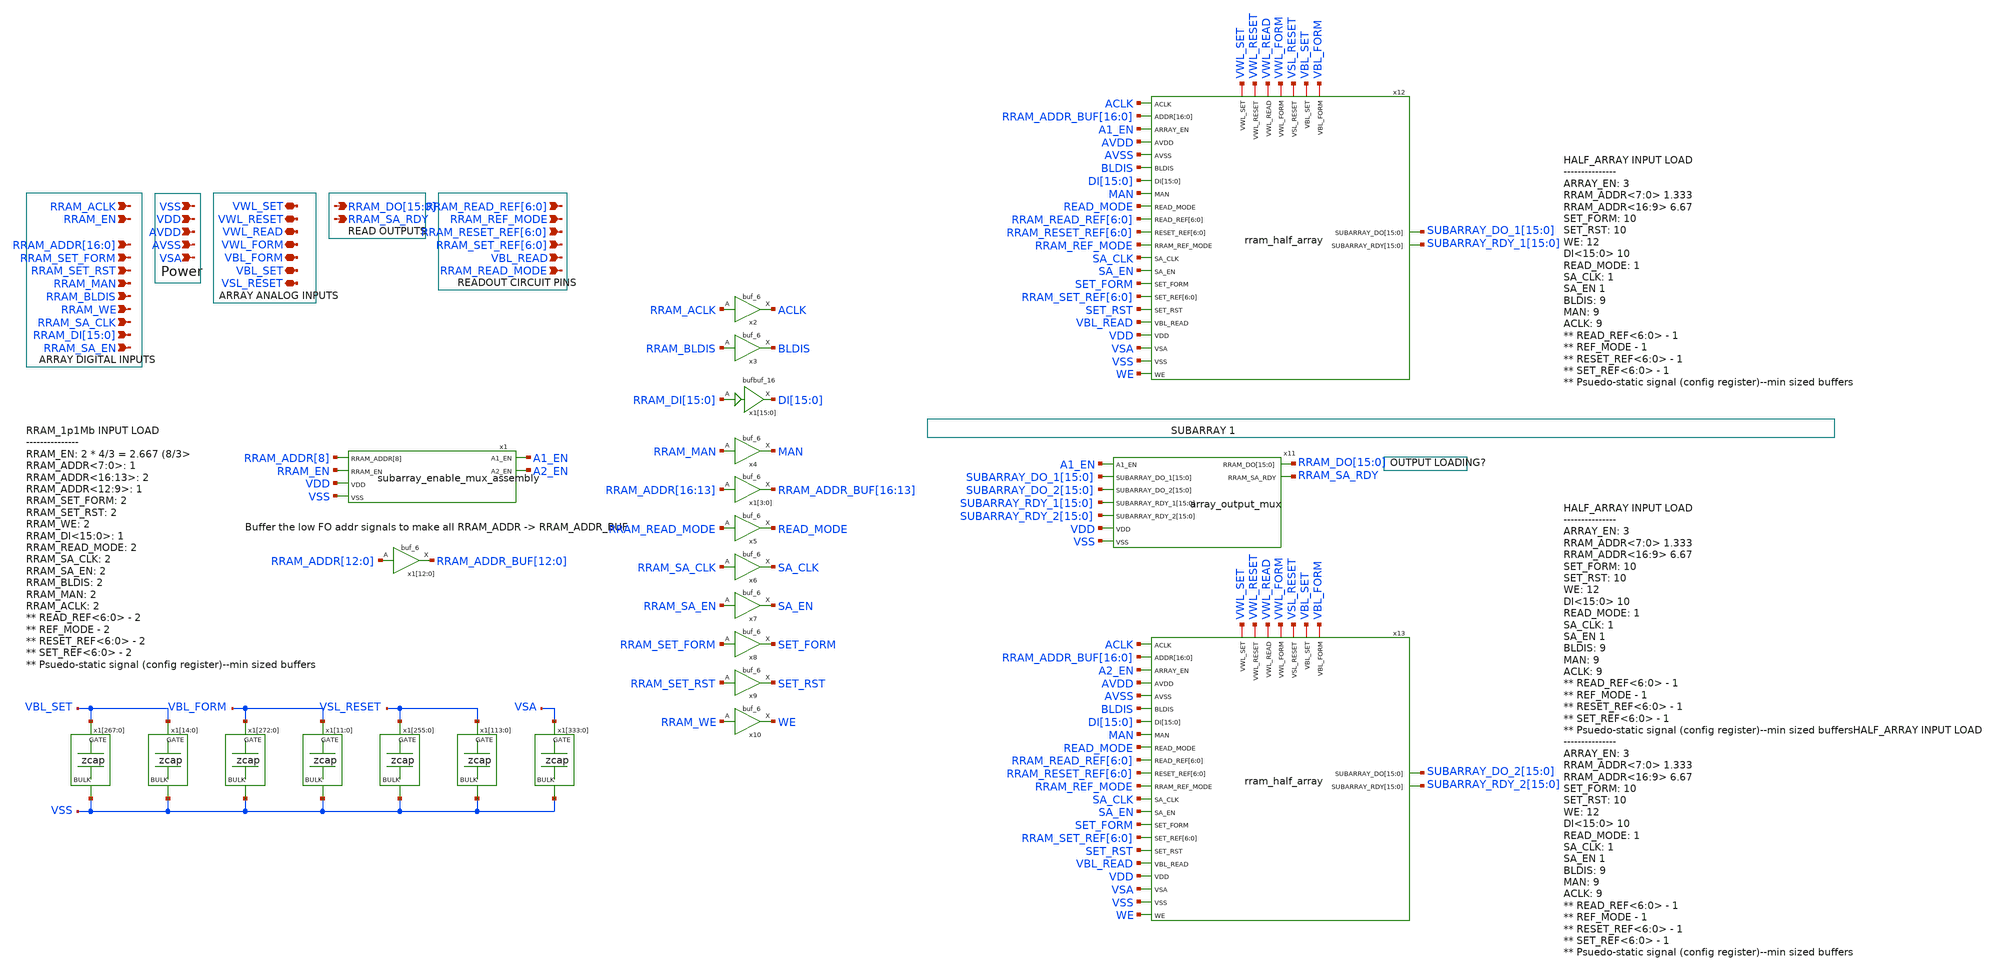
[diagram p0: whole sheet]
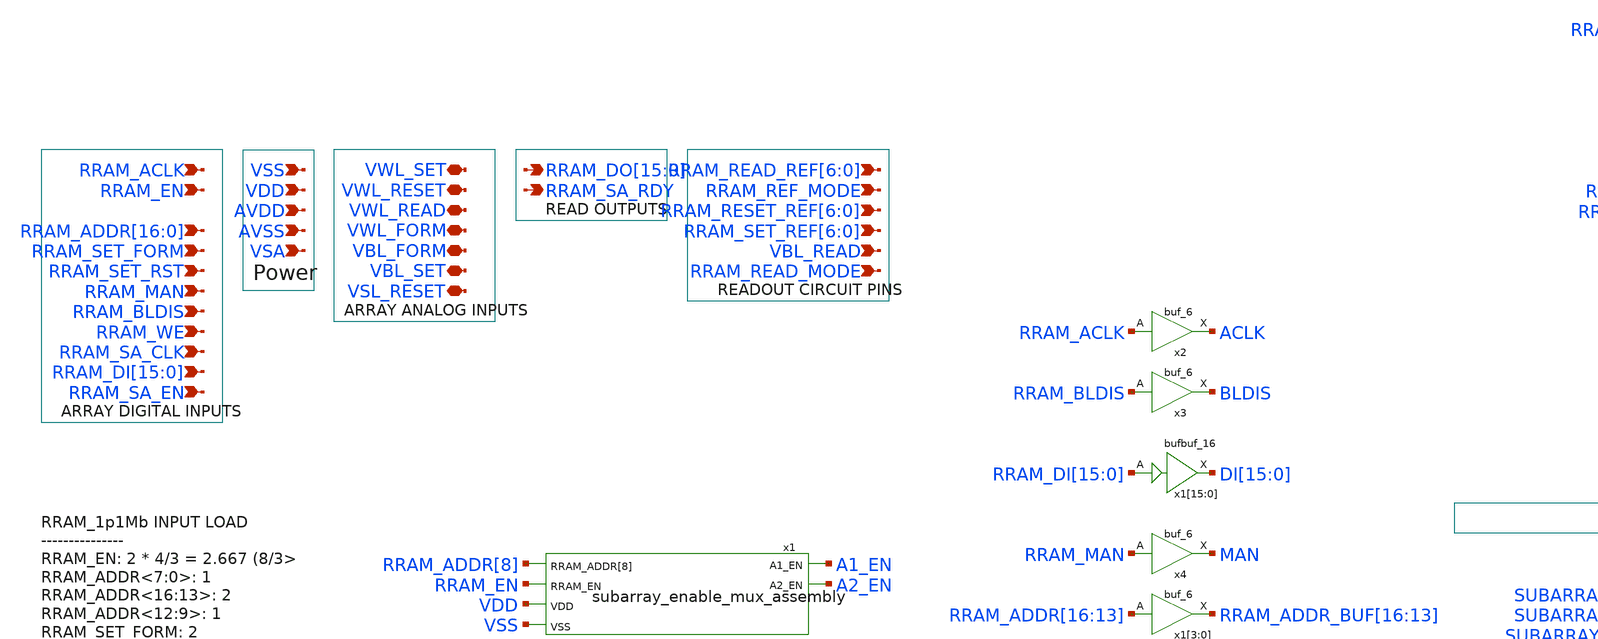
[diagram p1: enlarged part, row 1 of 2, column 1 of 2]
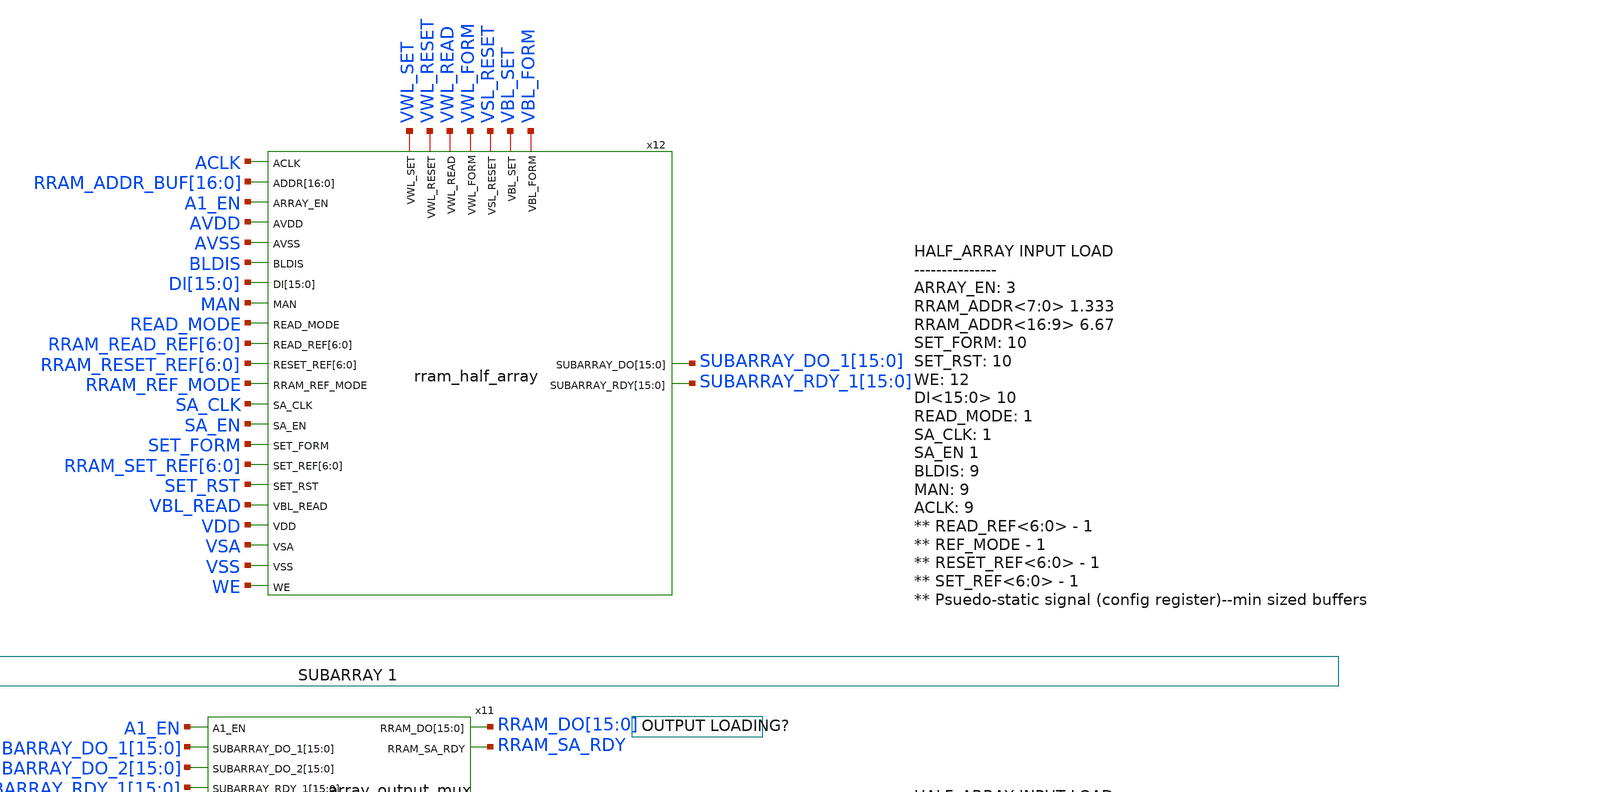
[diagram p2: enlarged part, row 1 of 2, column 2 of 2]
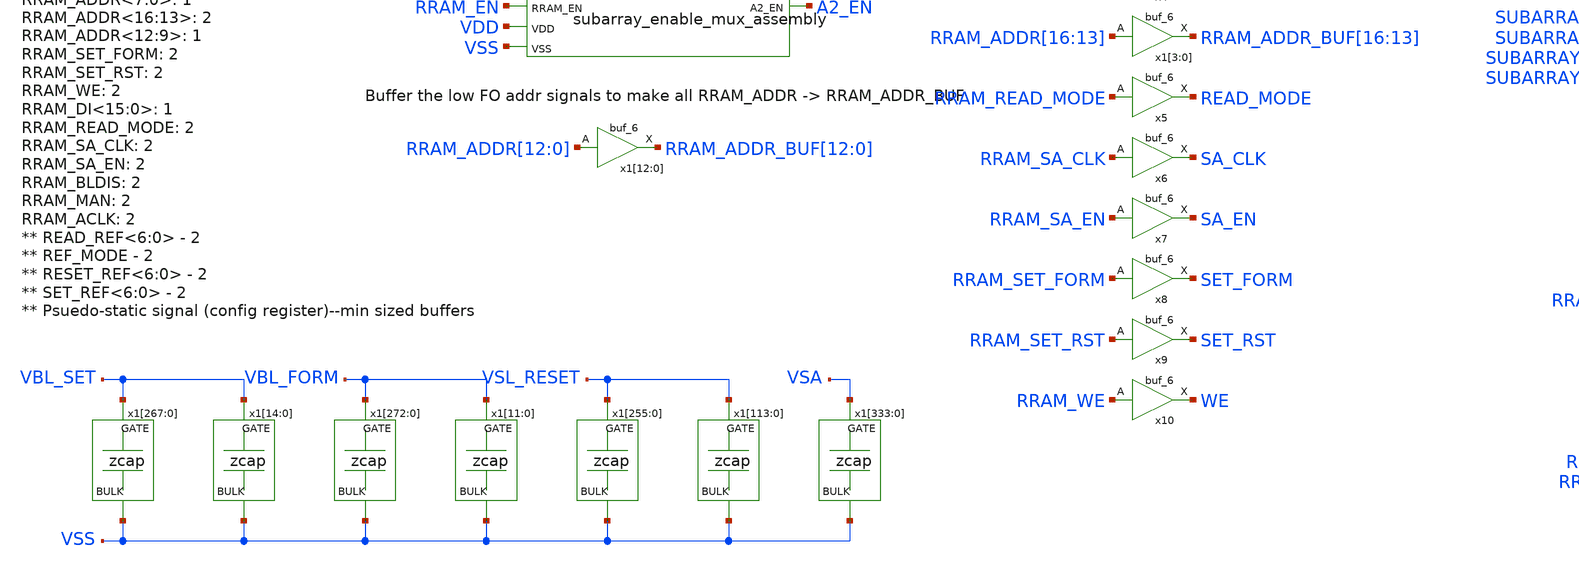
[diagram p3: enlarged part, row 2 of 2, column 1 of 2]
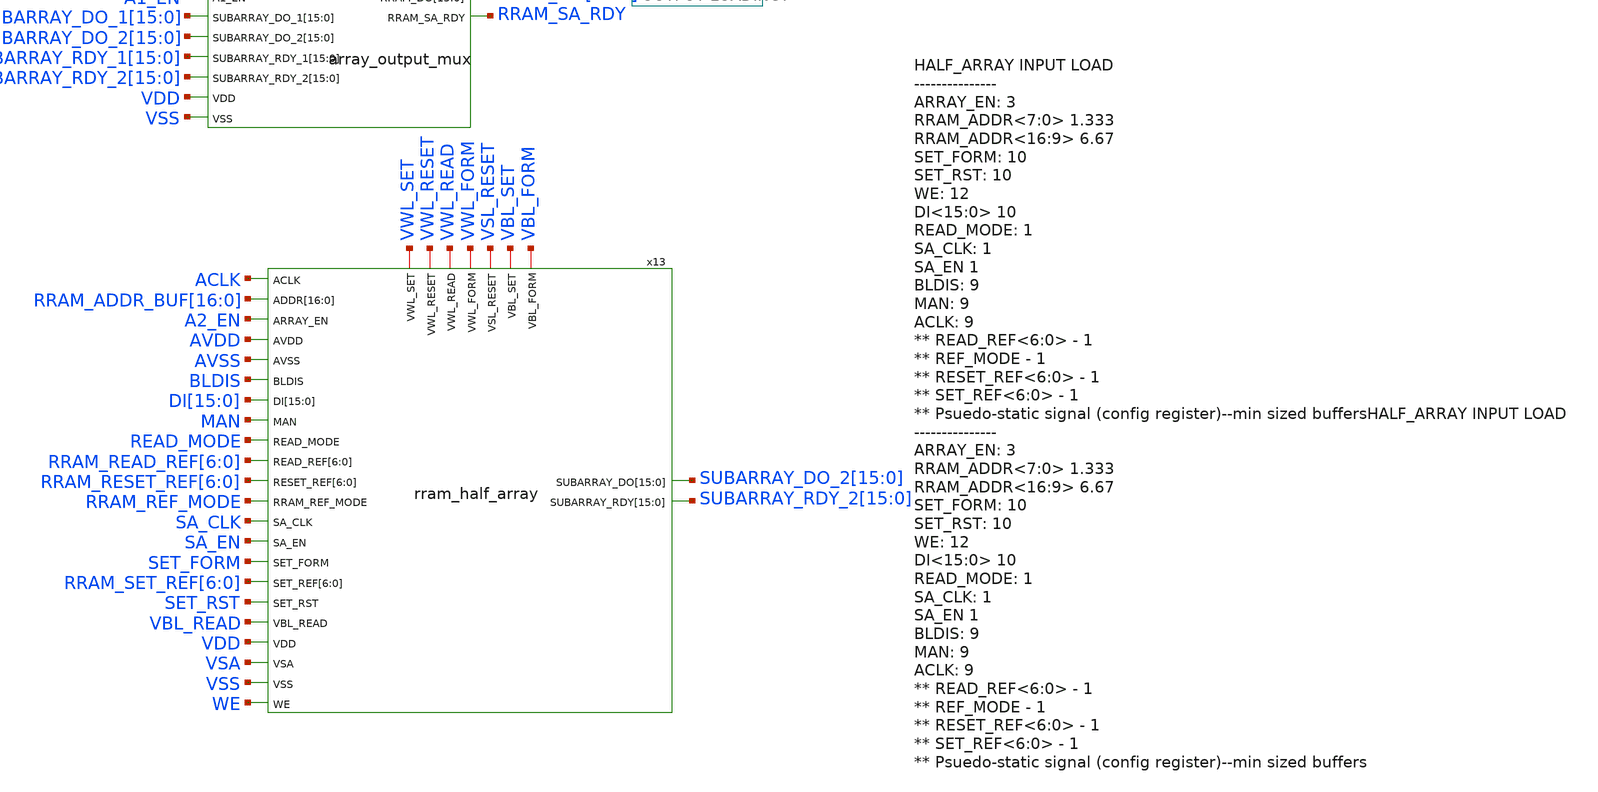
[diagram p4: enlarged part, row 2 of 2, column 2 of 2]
** sch_path: Top_Level_Array/rram_1pMb.sch
**.subckt rram_1pMb RRAM_ACLK RRAM_EN
*+ RRAM_ADDR[16],RRAM_ADDR[15],RRAM_ADDR[14],RRAM_ADDR[13],RRAM_ADDR[12],RRAM_ADDR[11],RRAM_ADDR[10],RRAM_ADDR[9],RRAM_ADDR[8],RRAM_ADDR[7],RRAM_ADDR[6],RRAM_ADDR[5],RRAM_ADDR[4],RRAM_ADDR[3],RRAM_ADDR[2],RRAM_ADDR[1],RRAM_ADDR[0] RRAM_SET_FORM RRAM_SET_RST RRAM_MAN RRAM_BLDIS RRAM_WE RRAM_SA_CLK
*+ RRAM_DI[15],RRAM_DI[14],RRAM_DI[13],RRAM_DI[12],RRAM_DI[11],RRAM_DI[10],RRAM_DI[9],RRAM_DI[8],RRAM_DI[7],RRAM_DI[6],RRAM_DI[5],RRAM_DI[4],RRAM_DI[3],RRAM_DI[2],RRAM_DI[1],RRAM_DI[0] RRAM_SA_EN VSS VDD AVDD AVSS VSA VWL_SET VWL_RESET VWL_READ VWL_FORM VBL_FORM VBL_SET VSL_RESET
*+ RRAM_DO[15],RRAM_DO[14],RRAM_DO[13],RRAM_DO[12],RRAM_DO[11],RRAM_DO[10],RRAM_DO[9],RRAM_DO[8],RRAM_DO[7],RRAM_DO[6],RRAM_DO[5],RRAM_DO[4],RRAM_DO[3],RRAM_DO[2],RRAM_DO[1],RRAM_DO[0] RRAM_SA_RDY
*+ RRAM_READ_REF[6],RRAM_READ_REF[5],RRAM_READ_REF[4],RRAM_READ_REF[3],RRAM_READ_REF[2],RRAM_READ_REF[1],RRAM_READ_REF[0] RRAM_REF_MODE
*+ RRAM_RESET_REF[6],RRAM_RESET_REF[5],RRAM_RESET_REF[4],RRAM_RESET_REF[3],RRAM_RESET_REF[2],RRAM_RESET_REF[1],RRAM_RESET_REF[0]
*+ RRAM_SET_REF[6],RRAM_SET_REF[5],RRAM_SET_REF[4],RRAM_SET_REF[3],RRAM_SET_REF[2],RRAM_SET_REF[1],RRAM_SET_REF[0] VBL_READ RRAM_READ_MODE
*.ipin RRAM_ACLK
*.ipin RRAM_EN
*.ipin
*+ RRAM_ADDR[16],RRAM_ADDR[15],RRAM_ADDR[14],RRAM_ADDR[13],RRAM_ADDR[12],RRAM_ADDR[11],RRAM_ADDR[10],RRAM_ADDR[9],RRAM_ADDR[8],RRAM_ADDR[7],RRAM_ADDR[6],RRAM_ADDR[5],RRAM_ADDR[4],RRAM_ADDR[3],RRAM_ADDR[2],RRAM_ADDR[1],RRAM_ADDR[0]
*.ipin RRAM_SET_FORM
*.ipin RRAM_SET_RST
*.ipin RRAM_MAN
*.ipin RRAM_BLDIS
*.ipin RRAM_WE
*.ipin RRAM_SA_CLK
*.ipin
*+ RRAM_DI[15],RRAM_DI[14],RRAM_DI[13],RRAM_DI[12],RRAM_DI[11],RRAM_DI[10],RRAM_DI[9],RRAM_DI[8],RRAM_DI[7],RRAM_DI[6],RRAM_DI[5],RRAM_DI[4],RRAM_DI[3],RRAM_DI[2],RRAM_DI[1],RRAM_DI[0]
*.ipin RRAM_SA_EN
*.ipin VSS
*.ipin VDD
*.ipin AVDD
*.ipin AVSS
*.ipin VSA
*.iopin VWL_SET
*.iopin VWL_RESET
*.iopin VWL_READ
*.iopin VWL_FORM
*.iopin VBL_FORM
*.iopin VBL_SET
*.iopin VSL_RESET
*.opin
*+ RRAM_DO[15],RRAM_DO[14],RRAM_DO[13],RRAM_DO[12],RRAM_DO[11],RRAM_DO[10],RRAM_DO[9],RRAM_DO[8],RRAM_DO[7],RRAM_DO[6],RRAM_DO[5],RRAM_DO[4],RRAM_DO[3],RRAM_DO[2],RRAM_DO[1],RRAM_DO[0]
*.opin RRAM_SA_RDY
*.ipin
*+ RRAM_READ_REF[6],RRAM_READ_REF[5],RRAM_READ_REF[4],RRAM_READ_REF[3],RRAM_READ_REF[2],RRAM_READ_REF[1],RRAM_READ_REF[0]
*.ipin RRAM_REF_MODE
*.ipin
*+ RRAM_RESET_REF[6],RRAM_RESET_REF[5],RRAM_RESET_REF[4],RRAM_RESET_REF[3],RRAM_RESET_REF[2],RRAM_RESET_REF[1],RRAM_RESET_REF[0]
*.ipin
*+ RRAM_SET_REF[6],RRAM_SET_REF[5],RRAM_SET_REF[4],RRAM_SET_REF[3],RRAM_SET_REF[2],RRAM_SET_REF[1],RRAM_SET_REF[0]
*.ipin VBL_READ
*.ipin RRAM_READ_MODE
x1[12] RRAM_ADDR[12] VSS VSS VDD VDD RRAM_ADDR_BUF[12] sky130_fd_sc_hd__buf_6
x1[11] RRAM_ADDR[11] VSS VSS VDD VDD RRAM_ADDR_BUF[11] sky130_fd_sc_hd__buf_6
x1[10] RRAM_ADDR[10] VSS VSS VDD VDD RRAM_ADDR_BUF[10] sky130_fd_sc_hd__buf_6
x1[9] RRAM_ADDR[9] VSS VSS VDD VDD RRAM_ADDR_BUF[9] sky130_fd_sc_hd__buf_6
x1[8] RRAM_ADDR[8] VSS VSS VDD VDD RRAM_ADDR_BUF[8] sky130_fd_sc_hd__buf_6
x1[7] RRAM_ADDR[7] VSS VSS VDD VDD RRAM_ADDR_BUF[7] sky130_fd_sc_hd__buf_6
x1[6] RRAM_ADDR[6] VSS VSS VDD VDD RRAM_ADDR_BUF[6] sky130_fd_sc_hd__buf_6
x1[5] RRAM_ADDR[5] VSS VSS VDD VDD RRAM_ADDR_BUF[5] sky130_fd_sc_hd__buf_6
x1[4] RRAM_ADDR[4] VSS VSS VDD VDD RRAM_ADDR_BUF[4] sky130_fd_sc_hd__buf_6
x1[3] RRAM_ADDR[3] VSS VSS VDD VDD RRAM_ADDR_BUF[3] sky130_fd_sc_hd__buf_6
x1[2] RRAM_ADDR[2] VSS VSS VDD VDD RRAM_ADDR_BUF[2] sky130_fd_sc_hd__buf_6
x1[1] RRAM_ADDR[1] VSS VSS VDD VDD RRAM_ADDR_BUF[1] sky130_fd_sc_hd__buf_6
x1[0] RRAM_ADDR[0] VSS VSS VDD VDD RRAM_ADDR_BUF[0] sky130_fd_sc_hd__buf_6
x1 VSS VDD A1_EN RRAM_EN RRAM_ADDR[8] A2_EN subarray_enable_mux_assembly
x1[15] RRAM_DI[15] VSS VSS VDD VDD DI[15] sky130_fd_sc_hd__bufbuf_16
x1[14] RRAM_DI[14] VSS VSS VDD VDD DI[14] sky130_fd_sc_hd__bufbuf_16
x1[13] RRAM_DI[13] VSS VSS VDD VDD DI[13] sky130_fd_sc_hd__bufbuf_16
x1[12] RRAM_DI[12] VSS VSS VDD VDD DI[12] sky130_fd_sc_hd__bufbuf_16
x1[11] RRAM_DI[11] VSS VSS VDD VDD DI[11] sky130_fd_sc_hd__bufbuf_16
x1[10] RRAM_DI[10] VSS VSS VDD VDD DI[10] sky130_fd_sc_hd__bufbuf_16
x1[9] RRAM_DI[9] VSS VSS VDD VDD DI[9] sky130_fd_sc_hd__bufbuf_16
x1[8] RRAM_DI[8] VSS VSS VDD VDD DI[8] sky130_fd_sc_hd__bufbuf_16
x1[7] RRAM_DI[7] VSS VSS VDD VDD DI[7] sky130_fd_sc_hd__bufbuf_16
x1[6] RRAM_DI[6] VSS VSS VDD VDD DI[6] sky130_fd_sc_hd__bufbuf_16
x1[5] RRAM_DI[5] VSS VSS VDD VDD DI[5] sky130_fd_sc_hd__bufbuf_16
x1[4] RRAM_DI[4] VSS VSS VDD VDD DI[4] sky130_fd_sc_hd__bufbuf_16
x1[3] RRAM_DI[3] VSS VSS VDD VDD DI[3] sky130_fd_sc_hd__bufbuf_16
x1[2] RRAM_DI[2] VSS VSS VDD VDD DI[2] sky130_fd_sc_hd__bufbuf_16
x1[1] RRAM_DI[1] VSS VSS VDD VDD DI[1] sky130_fd_sc_hd__bufbuf_16
x1[0] RRAM_DI[0] VSS VSS VDD VDD DI[0] sky130_fd_sc_hd__bufbuf_16
x2 RRAM_ACLK VSS VSS VDD VDD ACLK sky130_fd_sc_hd__buf_6
x3 RRAM_BLDIS VSS VSS VDD VDD BLDIS sky130_fd_sc_hd__buf_6
x4 RRAM_MAN VSS VSS VDD VDD MAN sky130_fd_sc_hd__buf_6
x1[3] RRAM_ADDR[16] VSS VSS VDD VDD RRAM_ADDR_BUF[16] sky130_fd_sc_hd__buf_6
x1[2] RRAM_ADDR[15] VSS VSS VDD VDD RRAM_ADDR_BUF[15] sky130_fd_sc_hd__buf_6
x1[1] RRAM_ADDR[14] VSS VSS VDD VDD RRAM_ADDR_BUF[14] sky130_fd_sc_hd__buf_6
x1[0] RRAM_ADDR[13] VSS VSS VDD VDD RRAM_ADDR_BUF[13] sky130_fd_sc_hd__buf_6
x5 RRAM_READ_MODE VSS VSS VDD VDD READ_MODE sky130_fd_sc_hd__buf_6
x6 RRAM_SA_CLK VSS VSS VDD VDD SA_CLK sky130_fd_sc_hd__buf_6
x7 RRAM_SA_EN VSS VSS VDD VDD SA_EN sky130_fd_sc_hd__buf_6
x8 RRAM_SET_FORM VSS VSS VDD VDD SET_FORM sky130_fd_sc_hd__buf_6
x9 RRAM_SET_RST VSS VSS VDD VDD SET_RST sky130_fd_sc_hd__buf_6
x10 RRAM_WE VSS VSS VDD VDD WE sky130_fd_sc_hd__buf_6
x11 VDD VSS A1_EN SUBARRAY_DO_1[15] SUBARRAY_DO_1[14] SUBARRAY_DO_1[13] SUBARRAY_DO_1[12]
+ SUBARRAY_DO_1[11] SUBARRAY_DO_1[10] SUBARRAY_DO_1[9] SUBARRAY_DO_1[8] SUBARRAY_DO_1[7] SUBARRAY_DO_1[6]
+ SUBARRAY_DO_1[5] SUBARRAY_DO_1[4] SUBARRAY_DO_1[3] SUBARRAY_DO_1[2] SUBARRAY_DO_1[1] SUBARRAY_DO_1[0]
+ SUBARRAY_RDY_1[15] SUBARRAY_RDY_1[14] SUBARRAY_RDY_1[13] SUBARRAY_RDY_1[12] SUBARRAY_RDY_1[11] SUBARRAY_RDY_1[10]
+ SUBARRAY_RDY_1[9] SUBARRAY_RDY_1[8] SUBARRAY_RDY_1[7] SUBARRAY_RDY_1[6] SUBARRAY_RDY_1[5] SUBARRAY_RDY_1[4]
+ SUBARRAY_RDY_1[3] SUBARRAY_RDY_1[2] SUBARRAY_RDY_1[1] SUBARRAY_RDY_1[0] SUBARRAY_DO_2[15] SUBARRAY_DO_2[14]
+ SUBARRAY_DO_2[13] SUBARRAY_DO_2[12] SUBARRAY_DO_2[11] SUBARRAY_DO_2[10] SUBARRAY_DO_2[9] SUBARRAY_DO_2[8]
+ SUBARRAY_DO_2[7] SUBARRAY_DO_2[6] SUBARRAY_DO_2[5] SUBARRAY_DO_2[4] SUBARRAY_DO_2[3] SUBARRAY_DO_2[2]
+ SUBARRAY_DO_2[1] SUBARRAY_DO_2[0] SUBARRAY_RDY_2[15] SUBARRAY_RDY_2[14] SUBARRAY_RDY_2[13] SUBARRAY_RDY_2[12]
+ SUBARRAY_RDY_2[11] SUBARRAY_RDY_2[10] SUBARRAY_RDY_2[9] SUBARRAY_RDY_2[8] SUBARRAY_RDY_2[7] SUBARRAY_RDY_2[6]
+ SUBARRAY_RDY_2[5] SUBARRAY_RDY_2[4] SUBARRAY_RDY_2[3] SUBARRAY_RDY_2[2] SUBARRAY_RDY_2[1] SUBARRAY_RDY_2[0]
+ RRAM_DO[15] RRAM_DO[14] RRAM_DO[13] RRAM_DO[12] RRAM_DO[11] RRAM_DO[10] RRAM_DO[9] RRAM_DO[8] RRAM_DO[7]
+ RRAM_DO[6] RRAM_DO[5] RRAM_DO[4] RRAM_DO[3] RRAM_DO[2] RRAM_DO[1] RRAM_DO[0] RRAM_SA_RDY array_output_mux
x12 SUBARRAY_DO_1[15] SUBARRAY_DO_1[14] SUBARRAY_DO_1[13] SUBARRAY_DO_1[12] SUBARRAY_DO_1[11]
+ SUBARRAY_DO_1[10] SUBARRAY_DO_1[9] SUBARRAY_DO_1[8] SUBARRAY_DO_1[7] SUBARRAY_DO_1[6] SUBARRAY_DO_1[5]
+ SUBARRAY_DO_1[4] SUBARRAY_DO_1[3] SUBARRAY_DO_1[2] SUBARRAY_DO_1[1] SUBARRAY_DO_1[0] VWL_SET VSS RRAM_READ_REF[6]
+ RRAM_READ_REF[5] RRAM_READ_REF[4] RRAM_READ_REF[3] RRAM_READ_REF[2] RRAM_READ_REF[1] RRAM_READ_REF[0] ACLK
+ RRAM_REF_MODE SUBARRAY_RDY_1[15] SUBARRAY_RDY_1[14] SUBARRAY_RDY_1[13] SUBARRAY_RDY_1[12] SUBARRAY_RDY_1[11]
+ SUBARRAY_RDY_1[10] SUBARRAY_RDY_1[9] SUBARRAY_RDY_1[8] SUBARRAY_RDY_1[7] SUBARRAY_RDY_1[6] SUBARRAY_RDY_1[5]
+ SUBARRAY_RDY_1[4] SUBARRAY_RDY_1[3] SUBARRAY_RDY_1[2] SUBARRAY_RDY_1[1] SUBARRAY_RDY_1[0] A1_EN VDD VWL_RESET
+ RRAM_RESET_REF[6] RRAM_RESET_REF[5] RRAM_RESET_REF[4] RRAM_RESET_REF[3] RRAM_RESET_REF[2] RRAM_RESET_REF[1]
+ RRAM_RESET_REF[0] AVDD RRAM_ADDR_BUF[16] RRAM_ADDR_BUF[15] RRAM_ADDR_BUF[14] RRAM_ADDR_BUF[13] RRAM_ADDR_BUF[12]
+ RRAM_ADDR_BUF[11] RRAM_ADDR_BUF[10] RRAM_ADDR_BUF[9] RRAM_ADDR_BUF[8] RRAM_ADDR_BUF[7] RRAM_ADDR_BUF[6]
+ RRAM_ADDR_BUF[5] RRAM_ADDR_BUF[4] RRAM_ADDR_BUF[3] RRAM_ADDR_BUF[2] RRAM_ADDR_BUF[1] RRAM_ADDR_BUF[0] VWL_READ AVSS
+ RRAM_SET_REF[6] RRAM_SET_REF[5] RRAM_SET_REF[4] RRAM_SET_REF[3] RRAM_SET_REF[2] RRAM_SET_REF[1] RRAM_SET_REF[0]
+ VWL_FORM SET_FORM SET_RST VBL_FORM VSA VBL_READ READ_MODE MAN VBL_SET VSL_RESET BLDIS WE SA_CLK DI[15]
+ DI[14] DI[13] DI[12] DI[11] DI[10] DI[9] DI[8] DI[7] DI[6] DI[5] DI[4] DI[3] DI[2] DI[1] DI[0] SA_EN
+ rram_half_array
x13 SUBARRAY_DO_2[15] SUBARRAY_DO_2[14] SUBARRAY_DO_2[13] SUBARRAY_DO_2[12] SUBARRAY_DO_2[11]
+ SUBARRAY_DO_2[10] SUBARRAY_DO_2[9] SUBARRAY_DO_2[8] SUBARRAY_DO_2[7] SUBARRAY_DO_2[6] SUBARRAY_DO_2[5]
+ SUBARRAY_DO_2[4] SUBARRAY_DO_2[3] SUBARRAY_DO_2[2] SUBARRAY_DO_2[1] SUBARRAY_DO_2[0] VWL_SET VSS RRAM_READ_REF[6]
+ RRAM_READ_REF[5] RRAM_READ_REF[4] RRAM_READ_REF[3] RRAM_READ_REF[2] RRAM_READ_REF[1] RRAM_READ_REF[0] ACLK
+ RRAM_REF_MODE SUBARRAY_RDY_2[15] SUBARRAY_RDY_2[14] SUBARRAY_RDY_2[13] SUBARRAY_RDY_2[12] SUBARRAY_RDY_2[11]
+ SUBARRAY_RDY_2[10] SUBARRAY_RDY_2[9] SUBARRAY_RDY_2[8] SUBARRAY_RDY_2[7] SUBARRAY_RDY_2[6] SUBARRAY_RDY_2[5]
+ SUBARRAY_RDY_2[4] SUBARRAY_RDY_2[3] SUBARRAY_RDY_2[2] SUBARRAY_RDY_2[1] SUBARRAY_RDY_2[0] A2_EN VDD VWL_RESET
+ RRAM_RESET_REF[6] RRAM_RESET_REF[5] RRAM_RESET_REF[4] RRAM_RESET_REF[3] RRAM_RESET_REF[2] RRAM_RESET_REF[1]
+ RRAM_RESET_REF[0] AVDD RRAM_ADDR_BUF[16] RRAM_ADDR_BUF[15] RRAM_ADDR_BUF[14] RRAM_ADDR_BUF[13] RRAM_ADDR_BUF[12]
+ RRAM_ADDR_BUF[11] RRAM_ADDR_BUF[10] RRAM_ADDR_BUF[9] RRAM_ADDR_BUF[8] RRAM_ADDR_BUF[7] RRAM_ADDR_BUF[6]
+ RRAM_ADDR_BUF[5] RRAM_ADDR_BUF[4] RRAM_ADDR_BUF[3] RRAM_ADDR_BUF[2] RRAM_ADDR_BUF[1] RRAM_ADDR_BUF[0] VWL_READ AVSS
+ RRAM_SET_REF[6] RRAM_SET_REF[5] RRAM_SET_REF[4] RRAM_SET_REF[3] RRAM_SET_REF[2] RRAM_SET_REF[1] RRAM_SET_REF[0]
+ VWL_FORM SET_FORM SET_RST VBL_FORM VSA VBL_READ READ_MODE MAN VBL_SET VSL_RESET BLDIS WE SA_CLK DI[15]
+ DI[14] DI[13] DI[12] DI[11] DI[10] DI[9] DI[8] DI[7] DI[6] DI[5] DI[4] DI[3] DI[2] DI[1] DI[0] SA_EN
+ rram_half_array
x1[267] VBL_SET VSS zcap
x1[266] VBL_SET VSS zcap
x1[265] VBL_SET VSS zcap
x1[264] VBL_SET VSS zcap
x1[263] VBL_SET VSS zcap
x1[262] VBL_SET VSS zcap
x1[261] VBL_SET VSS zcap
x1[260] VBL_SET VSS zcap
x1[259] VBL_SET VSS zcap
x1[258] VBL_SET VSS zcap
x1[257] VBL_SET VSS zcap
x1[256] VBL_SET VSS zcap
x1[255] VBL_SET VSS zcap
x1[254] VBL_SET VSS zcap
x1[253] VBL_SET VSS zcap
x1[252] VBL_SET VSS zcap
x1[251] VBL_SET VSS zcap
x1[250] VBL_SET VSS zcap
x1[249] VBL_SET VSS zcap
x1[248] VBL_SET VSS zcap
x1[247] VBL_SET VSS zcap
x1[246] VBL_SET VSS zcap
x1[245] VBL_SET VSS zcap
x1[244] VBL_SET VSS zcap
x1[243] VBL_SET VSS zcap
x1[242] VBL_SET VSS zcap
x1[241] VBL_SET VSS zcap
x1[240] VBL_SET VSS zcap
x1[239] VBL_SET VSS zcap
x1[238] VBL_SET VSS zcap
x1[237] VBL_SET VSS zcap
x1[236] VBL_SET VSS zcap
x1[235] VBL_SET VSS zcap
x1[234] VBL_SET VSS zcap
x1[233] VBL_SET VSS zcap
x1[232] VBL_SET VSS zcap
x1[231] VBL_SET VSS zcap
x1[230] VBL_SET VSS zcap
x1[229] VBL_SET VSS zcap
x1[228] VBL_SET VSS zcap
x1[227] VBL_SET VSS zcap
x1[226] VBL_SET VSS zcap
x1[225] VBL_SET VSS zcap
x1[224] VBL_SET VSS zcap
x1[223] VBL_SET VSS zcap
x1[222] VBL_SET VSS zcap
x1[221] VBL_SET VSS zcap
x1[220] VBL_SET VSS zcap
x1[219] VBL_SET VSS zcap
x1[218] VBL_SET VSS zcap
x1[217] VBL_SET VSS zcap
x1[216] VBL_SET VSS zcap
x1[215] VBL_SET VSS zcap
x1[214] VBL_SET VSS zcap
x1[213] VBL_SET VSS zcap
x1[212] VBL_SET VSS zcap
x1[211] VBL_SET VSS zcap
x1[210] VBL_SET VSS zcap
x1[209] VBL_SET VSS zcap
x1[208] VBL_SET VSS zcap
x1[207] VBL_SET VSS zcap
x1[206] VBL_SET VSS zcap
x1[205] VBL_SET VSS zcap
x1[204] VBL_SET VSS zcap
x1[203] VBL_SET VSS zcap
x1[202] VBL_SET VSS zcap
x1[201] VBL_SET VSS zcap
x1[200] VBL_SET VSS zcap
x1[199] VBL_SET VSS zcap
x1[198] VBL_SET VSS zcap
x1[197] VBL_SET VSS zcap
x1[196] VBL_SET VSS zcap
x1[195] VBL_SET VSS zcap
x1[194] VBL_SET VSS zcap
x1[193] VBL_SET VSS zcap
x1[192] VBL_SET VSS zcap
x1[191] VBL_SET VSS zcap
x1[190] VBL_SET VSS zcap
x1[189] VBL_SET VSS zcap
x1[188] VBL_SET VSS zcap
x1[187] VBL_SET VSS zcap
x1[186] VBL_SET VSS zcap
x1[185] VBL_SET VSS zcap
x1[184] VBL_SET VSS zcap
x1[183] VBL_SET VSS zcap
x1[182] VBL_SET VSS zcap
x1[181] VBL_SET VSS zcap
x1[180] VBL_SET VSS zcap
x1[179] VBL_SET VSS zcap
x1[178] VBL_SET VSS zcap
x1[177] VBL_SET VSS zcap
x1[176] VBL_SET VSS zcap
x1[175] VBL_SET VSS zcap
x1[174] VBL_SET VSS zcap
x1[173] VBL_SET VSS zcap
x1[172] VBL_SET VSS zcap
x1[171] VBL_SET VSS zcap
x1[170] VBL_SET VSS zcap
x1[169] VBL_SET VSS zcap
x1[168] VBL_SET VSS zcap
x1[167] VBL_SET VSS zcap
x1[166] VBL_SET VSS zcap
x1[165] VBL_SET VSS zcap
x1[164] VBL_SET VSS zcap
x1[163] VBL_SET VSS zcap
x1[162] VBL_SET VSS zcap
x1[161] VBL_SET VSS zcap
x1[160] VBL_SET VSS zcap
x1[159] VBL_SET VSS zcap
x1[158] VBL_SET VSS zcap
x1[157] VBL_SET VSS zcap
x1[156] VBL_SET VSS zcap
x1[155] VBL_SET VSS zcap
x1[154] VBL_SET VSS zcap
x1[153] VBL_SET VSS zcap
x1[152] VBL_SET VSS zcap
x1[151] VBL_SET VSS zcap
x1[150] VBL_SET VSS zcap
x1[149] VBL_SET VSS zcap
x1[148] VBL_SET VSS zcap
x1[147] VBL_SET VSS zcap
x1[146] VBL_SET VSS zcap
x1[145] VBL_SET VSS zcap
x1[144] VBL_SET VSS zcap
x1[143] VBL_SET VSS zcap
x1[142] VBL_SET VSS zcap
x1[141] VBL_SET VSS zcap
x1[140] VBL_SET VSS zcap
x1[139] VBL_SET VSS zcap
x1[138] VBL_SET VSS zcap
x1[137] VBL_SET VSS zcap
x1[136] VBL_SET VSS zcap
x1[135] VBL_SET VSS zcap
x1[134] VBL_SET VSS zcap
x1[133] VBL_SET VSS zcap
x1[132] VBL_SET VSS zcap
x1[131] VBL_SET VSS zcap
x1[130] VBL_SET VSS zcap
x1[129] VBL_SET VSS zcap
x1[128] VBL_SET VSS zcap
x1[127] VBL_SET VSS zcap
x1[126] VBL_SET VSS zcap
x1[125] VBL_SET VSS zcap
x1[124] VBL_SET VSS zcap
x1[123] VBL_SET VSS zcap
x1[122] VBL_SET VSS zcap
x1[121] VBL_SET VSS zcap
x1[120] VBL_SET VSS zcap
x1[119] VBL_SET VSS zcap
x1[118] VBL_SET VSS zcap
x1[117] VBL_SET VSS zcap
x1[116] VBL_SET VSS zcap
x1[115] VBL_SET VSS zcap
x1[114] VBL_SET VSS zcap
x1[113] VBL_SET VSS zcap
x1[112] VBL_SET VSS zcap
x1[111] VBL_SET VSS zcap
x1[110] VBL_SET VSS zcap
x1[109] VBL_SET VSS zcap
x1[108] VBL_SET VSS zcap
x1[107] VBL_SET VSS zcap
x1[106] VBL_SET VSS zcap
x1[105] VBL_SET VSS zcap
x1[104] VBL_SET VSS zcap
x1[103] VBL_SET VSS zcap
x1[102] VBL_SET VSS zcap
x1[101] VBL_SET VSS zcap
x1[100] VBL_SET VSS zcap
x1[99] VBL_SET VSS zcap
x1[98] VBL_SET VSS zcap
x1[97] VBL_SET VSS zcap
x1[96] VBL_SET VSS zcap
x1[95] VBL_SET VSS zcap
x1[94] VBL_SET VSS zcap
x1[93] VBL_SET VSS zcap
x1[92] VBL_SET VSS zcap
x1[91] VBL_SET VSS zcap
x1[90] VBL_SET VSS zcap
x1[89] VBL_SET VSS zcap
x1[88] VBL_SET VSS zcap
x1[87] VBL_SET VSS zcap
x1[86] VBL_SET VSS zcap
x1[85] VBL_SET VSS zcap
x1[84] VBL_SET VSS zcap
x1[83] VBL_SET VSS zcap
x1[82] VBL_SET VSS zcap
x1[81] VBL_SET VSS zcap
x1[80] VBL_SET VSS zcap
x1[79] VBL_SET VSS zcap
x1[78] VBL_SET VSS zcap
x1[77] VBL_SET VSS zcap
x1[76] VBL_SET VSS zcap
x1[75] VBL_SET VSS zcap
x1[74] VBL_SET VSS zcap
x1[73] VBL_SET VSS zcap
x1[72] VBL_SET VSS zcap
x1[71] VBL_SET VSS zcap
x1[70] VBL_SET VSS zcap
x1[69] VBL_SET VSS zcap
x1[68] VBL_SET VSS zcap
x1[67] VBL_SET VSS zcap
x1[66] VBL_SET VSS zcap
x1[65] VBL_SET VSS zcap
x1[64] VBL_SET VSS zcap
x1[63] VBL_SET VSS zcap
x1[62] VBL_SET VSS zcap
x1[61] VBL_SET VSS zcap
x1[60] VBL_SET VSS zcap
x1[59] VBL_SET VSS zcap
x1[58] VBL_SET VSS zcap
x1[57] VBL_SET VSS zcap
x1[56] VBL_SET VSS zcap
x1[55] VBL_SET VSS zcap
x1[54] VBL_SET VSS zcap
x1[53] VBL_SET VSS zcap
x1[52] VBL_SET VSS zcap
x1[51] VBL_SET VSS zcap
x1[50] VBL_SET VSS zcap
x1[49] VBL_SET VSS zcap
x1[48] VBL_SET VSS zcap
x1[47] VBL_SET VSS zcap
x1[46] VBL_SET VSS zcap
x1[45] VBL_SET VSS zcap
x1[44] VBL_SET VSS zcap
x1[43] VBL_SET VSS zcap
x1[42] VBL_SET VSS zcap
x1[41] VBL_SET VSS zcap
x1[40] VBL_SET VSS zcap
x1[39] VBL_SET VSS zcap
x1[38] VBL_SET VSS zcap
x1[37] VBL_SET VSS zcap
x1[36] VBL_SET VSS zcap
x1[35] VBL_SET VSS zcap
x1[34] VBL_SET VSS zcap
x1[33] VBL_SET VSS zcap
x1[32] VBL_SET VSS zcap
x1[31] VBL_SET VSS zcap
x1[30] VBL_SET VSS zcap
x1[29] VBL_SET VSS zcap
x1[28] VBL_SET VSS zcap
x1[27] VBL_SET VSS zcap
x1[26] VBL_SET VSS zcap
x1[25] VBL_SET VSS zcap
x1[24] VBL_SET VSS zcap
x1[23] VBL_SET VSS zcap
x1[22] VBL_SET VSS zcap
x1[21] VBL_SET VSS zcap
x1[20] VBL_SET VSS zcap
x1[19] VBL_SET VSS zcap
x1[18] VBL_SET VSS zcap
x1[17] VBL_SET VSS zcap
x1[16] VBL_SET VSS zcap
x1[15] VBL_SET VSS zcap
x1[14] VBL_SET VSS zcap
x1[13] VBL_SET VSS zcap
x1[12] VBL_SET VSS zcap
x1[11] VBL_SET VSS zcap
x1[10] VBL_SET VSS zcap
x1[9] VBL_SET VSS zcap
x1[8] VBL_SET VSS zcap
x1[7] VBL_SET VSS zcap
x1[6] VBL_SET VSS zcap
x1[5] VBL_SET VSS zcap
x1[4] VBL_SET VSS zcap
x1[3] VBL_SET VSS zcap
x1[2] VBL_SET VSS zcap
x1[1] VBL_SET VSS zcap
x1[0] VBL_SET VSS zcap
x1[272] VBL_FORM VSS zcap
x1[271] VBL_FORM VSS zcap
x1[270] VBL_FORM VSS zcap
x1[269] VBL_FORM VSS zcap
x1[268] VBL_FORM VSS zcap
x1[267] VBL_FORM VSS zcap
x1[266] VBL_FORM VSS zcap
x1[265] VBL_FORM VSS zcap
x1[264] VBL_FORM VSS zcap
x1[263] VBL_FORM VSS zcap
x1[262] VBL_FORM VSS zcap
x1[261] VBL_FORM VSS zcap
x1[260] VBL_FORM VSS zcap
x1[259] VBL_FORM VSS zcap
x1[258] VBL_FORM VSS zcap
x1[257] VBL_FORM VSS zcap
x1[256] VBL_FORM VSS zcap
x1[255] VBL_FORM VSS zcap
x1[254] VBL_FORM VSS zcap
x1[253] VBL_FORM VSS zcap
x1[252] VBL_FORM VSS zcap
x1[251] VBL_FORM VSS zcap
x1[250] VBL_FORM VSS zcap
x1[249] VBL_FORM VSS zcap
x1[248] VBL_FORM VSS zcap
x1[247] VBL_FORM VSS zcap
x1[246] VBL_FORM VSS zcap
x1[245] VBL_FORM VSS zcap
x1[244] VBL_FORM VSS zcap
x1[243] VBL_FORM VSS zcap
x1[242] VBL_FORM VSS zcap
x1[241] VBL_FORM VSS zcap
x1[240] VBL_FORM VSS zcap
x1[239] VBL_FORM VSS zcap
x1[238] VBL_FORM VSS zcap
x1[237] VBL_FORM VSS zcap
x1[236] VBL_FORM VSS zcap
x1[235] VBL_FORM VSS zcap
x1[234] VBL_FORM VSS zcap
x1[233] VBL_FORM VSS zcap
x1[232] VBL_FORM VSS zcap
x1[231] VBL_FORM VSS zcap
x1[230] VBL_FORM VSS zcap
x1[229] VBL_FORM VSS zcap
x1[228] VBL_FORM VSS zcap
x1[227] VBL_FORM VSS zcap
x1[226] VBL_FORM VSS zcap
x1[225] VBL_FORM VSS zcap
x1[224] VBL_FORM VSS zcap
x1[223] VBL_FORM VSS zcap
x1[222] VBL_FORM VSS zcap
x1[221] VBL_FORM VSS zcap
x1[220] VBL_FORM VSS zcap
x1[219] VBL_FORM VSS zcap
x1[218] VBL_FORM VSS zcap
x1[217] VBL_FORM VSS zcap
x1[216] VBL_FORM VSS zcap
x1[215] VBL_FORM VSS zcap
x1[214] VBL_FORM VSS zcap
x1[213] VBL_FORM VSS zcap
x1[212] VBL_FORM VSS zcap
x1[211] VBL_FORM VSS zcap
x1[210] VBL_FORM VSS zcap
x1[209] VBL_FORM VSS zcap
x1[208] VBL_FORM VSS zcap
x1[207] VBL_FORM VSS zcap
x1[206] VBL_FORM VSS zcap
x1[205] VBL_FORM VSS zcap
x1[204] VBL_FORM VSS zcap
x1[203] VBL_FORM VSS zcap
x1[202] VBL_FORM VSS zcap
x1[201] VBL_FORM VSS zcap
x1[200] VBL_FORM VSS zcap
x1[199] VBL_FORM VSS zcap
x1[198] VBL_FORM VSS zcap
x1[197] VBL_FORM VSS zcap
x1[196] VBL_FORM VSS zcap
x1[195] VBL_FORM VSS zcap
x1[194] VBL_FORM VSS zcap
x1[193] VBL_FORM VSS zcap
x1[192] VBL_FORM VSS zcap
x1[191] VBL_FORM VSS zcap
x1[190] VBL_FORM VSS zcap
x1[189] VBL_FORM VSS zcap
x1[188] VBL_FORM VSS zcap
x1[187] VBL_FORM VSS zcap
x1[186] VBL_FORM VSS zcap
x1[185] VBL_FORM VSS zcap
x1[184] VBL_FORM VSS zcap
x1[183] VBL_FORM VSS zcap
x1[182] VBL_FORM VSS zcap
x1[181] VBL_FORM VSS zcap
x1[180] VBL_FORM VSS zcap
x1[179] VBL_FORM VSS zcap
x1[178] VBL_FORM VSS zcap
x1[177] VBL_FORM VSS zcap
x1[176] VBL_FORM VSS zcap
x1[175] VBL_FORM VSS zcap
x1[174] VBL_FORM VSS zcap
x1[173] VBL_FORM VSS zcap
x1[172] VBL_FORM VSS zcap
x1[171] VBL_FORM VSS zcap
x1[170] VBL_FORM VSS zcap
x1[169] VBL_FORM VSS zcap
x1[168] VBL_FORM VSS zcap
x1[167] VBL_FORM VSS zcap
x1[166] VBL_FORM VSS zcap
x1[165] VBL_FORM VSS zcap
x1[164] VBL_FORM VSS zcap
x1[163] VBL_FORM VSS zcap
x1[162] VBL_FORM VSS zcap
x1[161] VBL_FORM VSS zcap
x1[160] VBL_FORM VSS zcap
x1[159] VBL_FORM VSS zcap
x1[158] VBL_FORM VSS zcap
x1[157] VBL_FORM VSS zcap
x1[156] VBL_FORM VSS zcap
x1[155] VBL_FORM VSS zcap
x1[154] VBL_FORM VSS zcap
x1[153] VBL_FORM VSS zcap
x1[152] VBL_FORM VSS zcap
x1[151] VBL_FORM VSS zcap
x1[150] VBL_FORM VSS zcap
x1[149] VBL_FORM VSS zcap
x1[148] VBL_FORM VSS zcap
x1[147] VBL_FORM VSS zcap
x1[146] VBL_FORM VSS zcap
x1[145] VBL_FORM VSS zcap
x1[144] VBL_FORM VSS zcap
x1[143] VBL_FORM VSS zcap
x1[142] VBL_FORM VSS zcap
x1[141] VBL_FORM VSS zcap
x1[140] VBL_FORM VSS zcap
x1[139] VBL_FORM VSS zcap
x1[138] VBL_FORM VSS zcap
x1[137] VBL_FORM VSS zcap
x1[136] VBL_FORM VSS zcap
x1[135] VBL_FORM VSS zcap
x1[134] VBL_FORM VSS zcap
x1[133] VBL_FORM VSS zcap
x1[132] VBL_FORM VSS zcap
x1[131] VBL_FORM VSS zcap
x1[130] VBL_FORM VSS zcap
x1[129] VBL_FORM VSS zcap
x1[128] VBL_FORM VSS zcap
x1[127] VBL_FORM VSS zcap
x1[126] VBL_FORM VSS zcap
x1[125] VBL_FORM VSS zcap
x1[124] VBL_FORM VSS zcap
x1[123] VBL_FORM VSS zcap
x1[122] VBL_FORM VSS zcap
x1[121] VBL_FORM VSS zcap
x1[120] VBL_FORM VSS zcap
x1[119] VBL_FORM VSS zcap
x1[118] VBL_FORM VSS zcap
x1[117] VBL_FORM VSS zcap
x1[116] VBL_FORM VSS zcap
x1[115] VBL_FORM VSS zcap
x1[114] VBL_FORM VSS zcap
x1[113] VBL_FORM VSS zcap
x1[112] VBL_FORM VSS zcap
x1[111] VBL_FORM VSS zcap
x1[110] VBL_FORM VSS zcap
x1[109] VBL_FORM VSS zcap
x1[108] VBL_FORM VSS zcap
x1[107] VBL_FORM VSS zcap
x1[106] VBL_FORM VSS zcap
x1[105] VBL_FORM VSS zcap
x1[104] VBL_FORM VSS zcap
x1[103] VBL_FORM VSS zcap
x1[102] VBL_FORM VSS zcap
x1[101] VBL_FORM VSS zcap
x1[100] VBL_FORM VSS zcap
x1[99] VBL_FORM VSS zcap
x1[98] VBL_FORM VSS zcap
x1[97] VBL_FORM VSS zcap
x1[96] VBL_FORM VSS zcap
x1[95] VBL_FORM VSS zcap
x1[94] VBL_FORM VSS zcap
x1[93] VBL_FORM VSS zcap
x1[92] VBL_FORM VSS zcap
x1[91] VBL_FORM VSS zcap
x1[90] VBL_FORM VSS zcap
x1[89] VBL_FORM VSS zcap
x1[88] VBL_FORM VSS zcap
x1[87] VBL_FORM VSS zcap
x1[86] VBL_FORM VSS zcap
x1[85] VBL_FORM VSS zcap
x1[84] VBL_FORM VSS zcap
x1[83] VBL_FORM VSS zcap
x1[82] VBL_FORM VSS zcap
x1[81] VBL_FORM VSS zcap
x1[80] VBL_FORM VSS zcap
x1[79] VBL_FORM VSS zcap
x1[78] VBL_FORM VSS zcap
x1[77] VBL_FORM VSS zcap
x1[76] VBL_FORM VSS zcap
x1[75] VBL_FORM VSS zcap
x1[74] VBL_FORM VSS zcap
x1[73] VBL_FORM VSS zcap
x1[72] VBL_FORM VSS zcap
x1[71] VBL_FORM VSS zcap
x1[70] VBL_FORM VSS zcap
x1[69] VBL_FORM VSS zcap
x1[68] VBL_FORM VSS zcap
x1[67] VBL_FORM VSS zcap
x1[66] VBL_FORM VSS zcap
x1[65] VBL_FORM VSS zcap
x1[64] VBL_FORM VSS zcap
x1[63] VBL_FORM VSS zcap
x1[62] VBL_FORM VSS zcap
x1[61] VBL_FORM VSS zcap
x1[60] VBL_FORM VSS zcap
x1[59] VBL_FORM VSS zcap
x1[58] VBL_FORM VSS zcap
x1[57] VBL_FORM VSS zcap
x1[56] VBL_FORM VSS zcap
x1[55] VBL_FORM VSS zcap
x1[54] VBL_FORM VSS zcap
x1[53] VBL_FORM VSS zcap
x1[52] VBL_FORM VSS zcap
x1[51] VBL_FORM VSS zcap
x1[50] VBL_FORM VSS zcap
x1[49] VBL_FORM VSS zcap
x1[48] VBL_FORM VSS zcap
x1[47] VBL_FORM VSS zcap
x1[46] VBL_FORM VSS zcap
x1[45] VBL_FORM VSS zcap
x1[44] VBL_FORM VSS zcap
x1[43] VBL_FORM VSS zcap
x1[42] VBL_FORM VSS zcap
x1[41] VBL_FORM VSS zcap
x1[40] VBL_FORM VSS zcap
x1[39] VBL_FORM VSS zcap
x1[38] VBL_FORM VSS zcap
x1[37] VBL_FORM VSS zcap
x1[36] VBL_FORM VSS zcap
x1[35] VBL_FORM VSS zcap
x1[34] VBL_FORM VSS zcap
x1[33] VBL_FORM VSS zcap
x1[32] VBL_FORM VSS zcap
x1[31] VBL_FORM VSS zcap
x1[30] VBL_FORM VSS zcap
x1[29] VBL_FORM VSS zcap
x1[28] VBL_FORM VSS zcap
x1[27] VBL_FORM VSS zcap
x1[26] VBL_FORM VSS zcap
x1[25] VBL_FORM VSS zcap
x1[24] VBL_FORM VSS zcap
x1[23] VBL_FORM VSS zcap
x1[22] VBL_FORM VSS zcap
x1[21] VBL_FORM VSS zcap
x1[20] VBL_FORM VSS zcap
x1[19] VBL_FORM VSS zcap
x1[18] VBL_FORM VSS zcap
x1[17] VBL_FORM VSS zcap
x1[16] VBL_FORM VSS zcap
x1[15] VBL_FORM VSS zcap
x1[14] VBL_FORM VSS zcap
x1[13] VBL_FORM VSS zcap
x1[12] VBL_FORM VSS zcap
x1[11] VBL_FORM VSS zcap
x1[10] VBL_FORM VSS zcap
x1[9] VBL_FORM VSS zcap
x1[8] VBL_FORM VSS zcap
x1[7] VBL_FORM VSS zcap
x1[6] VBL_FORM VSS zcap
x1[5] VBL_FORM VSS zcap
x1[4] VBL_FORM VSS zcap
x1[3] VBL_FORM VSS zcap
x1[2] VBL_FORM VSS zcap
x1[1] VBL_FORM VSS zcap
x1[0] VBL_FORM VSS zcap
x1[255] VSL_RESET VSS zcap
x1[254] VSL_RESET VSS zcap
x1[253] VSL_RESET VSS zcap
x1[252] VSL_RESET VSS zcap
x1[251] VSL_RESET VSS zcap
x1[250] VSL_RESET VSS zcap
x1[249] VSL_RESET VSS zcap
x1[248] VSL_RESET VSS zcap
x1[247] VSL_RESET VSS zcap
x1[246] VSL_RESET VSS zcap
x1[245] VSL_RESET VSS zcap
x1[244] VSL_RESET VSS zcap
x1[243] VSL_RESET VSS zcap
x1[242] VSL_RESET VSS zcap
x1[241] VSL_RESET VSS zcap
x1[240] VSL_RESET VSS zcap
x1[239] VSL_RESET VSS zcap
x1[238] VSL_RESET VSS zcap
x1[237] VSL_RESET VSS zcap
x1[236] VSL_RESET VSS zcap
x1[235] VSL_RESET VSS zcap
x1[234] VSL_RESET VSS zcap
x1[233] VSL_RESET VSS zcap
x1[232] VSL_RESET VSS zcap
x1[231] VSL_RESET VSS zcap
x1[230] VSL_RESET VSS zcap
x1[229] VSL_RESET VSS zcap
x1[228] VSL_RESET VSS zcap
x1[227] VSL_RESET VSS zcap
x1[226] VSL_RESET VSS zcap
x1[225] VSL_RESET VSS zcap
x1[224] VSL_RESET VSS zcap
x1[223] VSL_RESET VSS zcap
x1[222] VSL_RESET VSS zcap
x1[221] VSL_RESET VSS zcap
x1[220] VSL_RESET VSS zcap
x1[219] VSL_RESET VSS zcap
x1[218] VSL_RESET VSS zcap
x1[217] VSL_RESET VSS zcap
x1[216] VSL_RESET VSS zcap
x1[215] VSL_RESET VSS zcap
x1[214] VSL_RESET VSS zcap
x1[213] VSL_RESET VSS zcap
x1[212] VSL_RESET VSS zcap
x1[211] VSL_RESET VSS zcap
x1[210] VSL_RESET VSS zcap
x1[209] VSL_RESET VSS zcap
x1[208] VSL_RESET VSS zcap
x1[207] VSL_RESET VSS zcap
x1[206] VSL_RESET VSS zcap
x1[205] VSL_RESET VSS zcap
x1[204] VSL_RESET VSS zcap
x1[203] VSL_RESET VSS zcap
x1[202] VSL_RESET VSS zcap
x1[201] VSL_RESET VSS zcap
x1[200] VSL_RESET VSS zcap
x1[199] VSL_RESET VSS zcap
x1[198] VSL_RESET VSS zcap
x1[197] VSL_RESET VSS zcap
x1[196] VSL_RESET VSS zcap
x1[195] VSL_RESET VSS zcap
x1[194] VSL_RESET VSS zcap
x1[193] VSL_RESET VSS zcap
x1[192] VSL_RESET VSS zcap
x1[191] VSL_RESET VSS zcap
x1[190] VSL_RESET VSS zcap
x1[189] VSL_RESET VSS zcap
x1[188] VSL_RESET VSS zcap
x1[187] VSL_RESET VSS zcap
x1[186] VSL_RESET VSS zcap
x1[185] VSL_RESET VSS zcap
x1[184] VSL_RESET VSS zcap
x1[183] VSL_RESET VSS zcap
x1[182] VSL_RESET VSS zcap
x1[181] VSL_RESET VSS zcap
x1[180] VSL_RESET VSS zcap
x1[179] VSL_RESET VSS zcap
x1[178] VSL_RESET VSS zcap
x1[177] VSL_RESET VSS zcap
x1[176] VSL_RESET VSS zcap
x1[175] VSL_RESET VSS zcap
x1[174] VSL_RESET VSS zcap
x1[173] VSL_RESET VSS zcap
x1[172] VSL_RESET VSS zcap
x1[171] VSL_RESET VSS zcap
x1[170] VSL_RESET VSS zcap
x1[169] VSL_RESET VSS zcap
x1[168] VSL_RESET VSS zcap
x1[167] VSL_RESET VSS zcap
x1[166] VSL_RESET VSS zcap
x1[165] VSL_RESET VSS zcap
x1[164] VSL_RESET VSS zcap
x1[163] VSL_RESET VSS zcap
x1[162] VSL_RESET VSS zcap
x1[161] VSL_RESET VSS zcap
x1[160] VSL_RESET VSS zcap
x1[159] VSL_RESET VSS zcap
x1[158] VSL_RESET VSS zcap
x1[157] VSL_RESET VSS zcap
x1[156] VSL_RESET VSS zcap
x1[155] VSL_RESET VSS zcap
x1[154] VSL_RESET VSS zcap
x1[153] VSL_RESET VSS zcap
x1[152] VSL_RESET VSS zcap
x1[151] VSL_RESET VSS zcap
x1[150] VSL_RESET VSS zcap
x1[149] VSL_RESET VSS zcap
x1[148] VSL_RESET VSS zcap
x1[147] VSL_RESET VSS zcap
x1[146] VSL_RESET VSS zcap
x1[145] VSL_RESET VSS zcap
x1[144] VSL_RESET VSS zcap
x1[143] VSL_RESET VSS zcap
x1[142] VSL_RESET VSS zcap
x1[141] VSL_RESET VSS zcap
x1[140] VSL_RESET VSS zcap
x1[139] VSL_RESET VSS zcap
x1[138] VSL_RESET VSS zcap
x1[137] VSL_RESET VSS zcap
x1[136] VSL_RESET VSS zcap
x1[135] VSL_RESET VSS zcap
x1[134] VSL_RESET VSS zcap
x1[133] VSL_RESET VSS zcap
x1[132] VSL_RESET VSS zcap
x1[131] VSL_RESET VSS zcap
x1[130] VSL_RESET VSS zcap
x1[129] VSL_RESET VSS zcap
x1[128] VSL_RESET VSS zcap
x1[127] VSL_RESET VSS zcap
x1[126] VSL_RESET VSS zcap
x1[125] VSL_RESET VSS zcap
x1[124] VSL_RESET VSS zcap
x1[123] VSL_RESET VSS zcap
x1[122] VSL_RESET VSS zcap
x1[121] VSL_RESET VSS zcap
x1[120] VSL_RESET VSS zcap
x1[119] VSL_RESET VSS zcap
x1[118] VSL_RESET VSS zcap
x1[117] VSL_RESET VSS zcap
x1[116] VSL_RESET VSS zcap
x1[115] VSL_RESET VSS zcap
x1[114] VSL_RESET VSS zcap
x1[113] VSL_RESET VSS zcap
x1[112] VSL_RESET VSS zcap
x1[111] VSL_RESET VSS zcap
x1[110] VSL_RESET VSS zcap
x1[109] VSL_RESET VSS zcap
x1[108] VSL_RESET VSS zcap
x1[107] VSL_RESET VSS zcap
x1[106] VSL_RESET VSS zcap
x1[105] VSL_RESET VSS zcap
x1[104] VSL_RESET VSS zcap
x1[103] VSL_RESET VSS zcap
x1[102] VSL_RESET VSS zcap
x1[101] VSL_RESET VSS zcap
x1[100] VSL_RESET VSS zcap
x1[99] VSL_RESET VSS zcap
x1[98] VSL_RESET VSS zcap
x1[97] VSL_RESET VSS zcap
x1[96] VSL_RESET VSS zcap
x1[95] VSL_RESET VSS zcap
x1[94] VSL_RESET VSS zcap
x1[93] VSL_RESET VSS zcap
x1[92] VSL_RESET VSS zcap
x1[91] VSL_RESET VSS zcap
x1[90] VSL_RESET VSS zcap
x1[89] VSL_RESET VSS zcap
x1[88] VSL_RESET VSS zcap
x1[87] VSL_RESET VSS zcap
x1[86] VSL_RESET VSS zcap
x1[85] VSL_RESET VSS zcap
x1[84] VSL_RESET VSS zcap
x1[83] VSL_RESET VSS zcap
x1[82] VSL_RESET VSS zcap
x1[81] VSL_RESET VSS zcap
x1[80] VSL_RESET VSS zcap
x1[79] VSL_RESET VSS zcap
x1[78] VSL_RESET VSS zcap
x1[77] VSL_RESET VSS zcap
x1[76] VSL_RESET VSS zcap
x1[75] VSL_RESET VSS zcap
x1[74] VSL_RESET VSS zcap
x1[73] VSL_RESET VSS zcap
x1[72] VSL_RESET VSS zcap
x1[71] VSL_RESET VSS zcap
x1[70] VSL_RESET VSS zcap
x1[69] VSL_RESET VSS zcap
x1[68] VSL_RESET VSS zcap
x1[67] VSL_RESET VSS zcap
x1[66] VSL_RESET VSS zcap
x1[65] VSL_RESET VSS zcap
x1[64] VSL_RESET VSS zcap
x1[63] VSL_RESET VSS zcap
x1[62] VSL_RESET VSS zcap
x1[61] VSL_RESET VSS zcap
x1[60] VSL_RESET VSS zcap
x1[59] VSL_RESET VSS zcap
x1[58] VSL_RESET VSS zcap
x1[57] VSL_RESET VSS zcap
x1[56] VSL_RESET VSS zcap
x1[55] VSL_RESET VSS zcap
x1[54] VSL_RESET VSS zcap
x1[53] VSL_RESET VSS zcap
x1[52] VSL_RESET VSS zcap
x1[51] VSL_RESET VSS zcap
x1[50] VSL_RESET VSS zcap
x1[49] VSL_RESET VSS zcap
x1[48] VSL_RESET VSS zcap
x1[47] VSL_RESET VSS zcap
x1[46] VSL_RESET VSS zcap
x1[45] VSL_RESET VSS zcap
x1[44] VSL_RESET VSS zcap
x1[43] VSL_RESET VSS zcap
x1[42] VSL_RESET VSS zcap
x1[41] VSL_RESET VSS zcap
x1[40] VSL_RESET VSS zcap
x1[39] VSL_RESET VSS zcap
x1[38] VSL_RESET VSS zcap
x1[37] VSL_RESET VSS zcap
x1[36] VSL_RESET VSS zcap
x1[35] VSL_RESET VSS zcap
x1[34] VSL_RESET VSS zcap
x1[33] VSL_RESET VSS zcap
x1[32] VSL_RESET VSS zcap
x1[31] VSL_RESET VSS zcap
x1[30] VSL_RESET VSS zcap
x1[29] VSL_RESET VSS zcap
x1[28] VSL_RESET VSS zcap
x1[27] VSL_RESET VSS zcap
x1[26] VSL_RESET VSS zcap
x1[25] VSL_RESET VSS zcap
x1[24] VSL_RESET VSS zcap
x1[23] VSL_RESET VSS zcap
x1[22] VSL_RESET VSS zcap
x1[21] VSL_RESET VSS zcap
x1[20] VSL_RESET VSS zcap
x1[19] VSL_RESET VSS zcap
x1[18] VSL_RESET VSS zcap
x1[17] VSL_RESET VSS zcap
x1[16] VSL_RESET VSS zcap
x1[15] VSL_RESET VSS zcap
x1[14] VSL_RESET VSS zcap
x1[13] VSL_RESET VSS zcap
x1[12] VSL_RESET VSS zcap
x1[11] VSL_RESET VSS zcap
x1[10] VSL_RESET VSS zcap
x1[9] VSL_RESET VSS zcap
x1[8] VSL_RESET VSS zcap
x1[7] VSL_RESET VSS zcap
x1[6] VSL_RESET VSS zcap
x1[5] VSL_RESET VSS zcap
x1[4] VSL_RESET VSS zcap
x1[3] VSL_RESET VSS zcap
x1[2] VSL_RESET VSS zcap
x1[1] VSL_RESET VSS zcap
x1[0] VSL_RESET VSS zcap
x1[14] VBL_SET VSS zcap
x1[13] VBL_SET VSS zcap
x1[12] VBL_SET VSS zcap
x1[11] VBL_SET VSS zcap
x1[10] VBL_SET VSS zcap
x1[9] VBL_SET VSS zcap
x1[8] VBL_SET VSS zcap
x1[7] VBL_SET VSS zcap
x1[6] VBL_SET VSS zcap
x1[5] VBL_SET VSS zcap
x1[4] VBL_SET VSS zcap
x1[3] VBL_SET VSS zcap
x1[2] VBL_SET VSS zcap
x1[1] VBL_SET VSS zcap
x1[0] VBL_SET VSS zcap
x1[11] VBL_FORM VSS zcap
x1[10] VBL_FORM VSS zcap
x1[9] VBL_FORM VSS zcap
x1[8] VBL_FORM VSS zcap
x1[7] VBL_FORM VSS zcap
x1[6] VBL_FORM VSS zcap
x1[5] VBL_FORM VSS zcap
x1[4] VBL_FORM VSS zcap
x1[3] VBL_FORM VSS zcap
x1[2] VBL_FORM VSS zcap
x1[1] VBL_FORM VSS zcap
x1[0] VBL_FORM VSS zcap
x1[113] VSL_RESET VSS zcap
x1[112] VSL_RESET VSS zcap
x1[111] VSL_RESET VSS zcap
x1[110] VSL_RESET VSS zcap
x1[109] VSL_RESET VSS zcap
x1[108] VSL_RESET VSS zcap
x1[107] VSL_RESET VSS zcap
x1[106] VSL_RESET VSS zcap
x1[105] VSL_RESET VSS zcap
x1[104] VSL_RESET VSS zcap
x1[103] VSL_RESET VSS zcap
x1[102] VSL_RESET VSS zcap
x1[101] VSL_RESET VSS zcap
x1[100] VSL_RESET VSS zcap
x1[99] VSL_RESET VSS zcap
x1[98] VSL_RESET VSS zcap
x1[97] VSL_RESET VSS zcap
x1[96] VSL_RESET VSS zcap
x1[95] VSL_RESET VSS zcap
x1[94] VSL_RESET VSS zcap
x1[93] VSL_RESET VSS zcap
x1[92] VSL_RESET VSS zcap
x1[91] VSL_RESET VSS zcap
x1[90] VSL_RESET VSS zcap
x1[89] VSL_RESET VSS zcap
x1[88] VSL_RESET VSS zcap
x1[87] VSL_RESET VSS zcap
x1[86] VSL_RESET VSS zcap
x1[85] VSL_RESET VSS zcap
x1[84] VSL_RESET VSS zcap
x1[83] VSL_RESET VSS zcap
x1[82] VSL_RESET VSS zcap
x1[81] VSL_RESET VSS zcap
x1[80] VSL_RESET VSS zcap
x1[79] VSL_RESET VSS zcap
x1[78] VSL_RESET VSS zcap
x1[77] VSL_RESET VSS zcap
x1[76] VSL_RESET VSS zcap
x1[75] VSL_RESET VSS zcap
x1[74] VSL_RESET VSS zcap
x1[73] VSL_RESET VSS zcap
x1[72] VSL_RESET VSS zcap
x1[71] VSL_RESET VSS zcap
x1[70] VSL_RESET VSS zcap
x1[69] VSL_RESET VSS zcap
x1[68] VSL_RESET VSS zcap
x1[67] VSL_RESET VSS zcap
x1[66] VSL_RESET VSS zcap
x1[65] VSL_RESET VSS zcap
x1[64] VSL_RESET VSS zcap
x1[63] VSL_RESET VSS zcap
x1[62] VSL_RESET VSS zcap
x1[61] VSL_RESET VSS zcap
x1[60] VSL_RESET VSS zcap
x1[59] VSL_RESET VSS zcap
x1[58] VSL_RESET VSS zcap
x1[57] VSL_RESET VSS zcap
x1[56] VSL_RESET VSS zcap
x1[55] VSL_RESET VSS zcap
x1[54] VSL_RESET VSS zcap
x1[53] VSL_RESET VSS zcap
x1[52] VSL_RESET VSS zcap
x1[51] VSL_RESET VSS zcap
x1[50] VSL_RESET VSS zcap
x1[49] VSL_RESET VSS zcap
x1[48] VSL_RESET VSS zcap
x1[47] VSL_RESET VSS zcap
x1[46] VSL_RESET VSS zcap
x1[45] VSL_RESET VSS zcap
x1[44] VSL_RESET VSS zcap
x1[43] VSL_RESET VSS zcap
x1[42] VSL_RESET VSS zcap
x1[41] VSL_RESET VSS zcap
x1[40] VSL_RESET VSS zcap
x1[39] VSL_RESET VSS zcap
x1[38] VSL_RESET VSS zcap
x1[37] VSL_RESET VSS zcap
x1[36] VSL_RESET VSS zcap
x1[35] VSL_RESET VSS zcap
x1[34] VSL_RESET VSS zcap
x1[33] VSL_RESET VSS zcap
x1[32] VSL_RESET VSS zcap
x1[31] VSL_RESET VSS zcap
x1[30] VSL_RESET VSS zcap
x1[29] VSL_RESET VSS zcap
x1[28] VSL_RESET VSS zcap
x1[27] VSL_RESET VSS zcap
x1[26] VSL_RESET VSS zcap
x1[25] VSL_RESET VSS zcap
x1[24] VSL_RESET VSS zcap
x1[23] VSL_RESET VSS zcap
x1[22] VSL_RESET VSS zcap
x1[21] VSL_RESET VSS zcap
x1[20] VSL_RESET VSS zcap
x1[19] VSL_RESET VSS zcap
x1[18] VSL_RESET VSS zcap
x1[17] VSL_RESET VSS zcap
x1[16] VSL_RESET VSS zcap
x1[15] VSL_RESET VSS zcap
x1[14] VSL_RESET VSS zcap
x1[13] VSL_RESET VSS zcap
x1[12] VSL_RESET VSS zcap
x1[11] VSL_RESET VSS zcap
x1[10] VSL_RESET VSS zcap
x1[9] VSL_RESET VSS zcap
x1[8] VSL_RESET VSS zcap
x1[7] VSL_RESET VSS zcap
x1[6] VSL_RESET VSS zcap
x1[5] VSL_RESET VSS zcap
x1[4] VSL_RESET VSS zcap
x1[3] VSL_RESET VSS zcap
x1[2] VSL_RESET VSS zcap
x1[1] VSL_RESET VSS zcap
x1[0] VSL_RESET VSS zcap
x1[333] VSA VSS zcap
x1[332] VSA VSS zcap
x1[331] VSA VSS zcap
x1[330] VSA VSS zcap
x1[329] VSA VSS zcap
x1[328] VSA VSS zcap
x1[327] VSA VSS zcap
x1[326] VSA VSS zcap
x1[325] VSA VSS zcap
x1[324] VSA VSS zcap
x1[323] VSA VSS zcap
x1[322] VSA VSS zcap
x1[321] VSA VSS zcap
x1[320] VSA VSS zcap
x1[319] VSA VSS zcap
x1[318] VSA VSS zcap
x1[317] VSA VSS zcap
x1[316] VSA VSS zcap
x1[315] VSA VSS zcap
x1[314] VSA VSS zcap
x1[313] VSA VSS zcap
x1[312] VSA VSS zcap
x1[311] VSA VSS zcap
x1[310] VSA VSS zcap
x1[309] VSA VSS zcap
x1[308] VSA VSS zcap
x1[307] VSA VSS zcap
x1[306] VSA VSS zcap
x1[305] VSA VSS zcap
x1[304] VSA VSS zcap
x1[303] VSA VSS zcap
x1[302] VSA VSS zcap
x1[301] VSA VSS zcap
x1[300] VSA VSS zcap
x1[299] VSA VSS zcap
x1[298] VSA VSS zcap
x1[297] VSA VSS zcap
x1[296] VSA VSS zcap
x1[295] VSA VSS zcap
x1[294] VSA VSS zcap
x1[293] VSA VSS zcap
x1[292] VSA VSS zcap
x1[291] VSA VSS zcap
x1[290] VSA VSS zcap
x1[289] VSA VSS zcap
x1[288] VSA VSS zcap
x1[287] VSA VSS zcap
x1[286] VSA VSS zcap
x1[285] VSA VSS zcap
x1[284] VSA VSS zcap
x1[283] VSA VSS zcap
x1[282] VSA VSS zcap
x1[281] VSA VSS zcap
x1[280] VSA VSS zcap
x1[279] VSA VSS zcap
x1[278] VSA VSS zcap
x1[277] VSA VSS zcap
x1[276] VSA VSS zcap
x1[275] VSA VSS zcap
x1[274] VSA VSS zcap
x1[273] VSA VSS zcap
x1[272] VSA VSS zcap
x1[271] VSA VSS zcap
x1[270] VSA VSS zcap
x1[269] VSA VSS zcap
x1[268] VSA VSS zcap
x1[267] VSA VSS zcap
x1[266] VSA VSS zcap
x1[265] VSA VSS zcap
x1[264] VSA VSS zcap
x1[263] VSA VSS zcap
x1[262] VSA VSS zcap
x1[261] VSA VSS zcap
x1[260] VSA VSS zcap
x1[259] VSA VSS zcap
x1[258] VSA VSS zcap
x1[257] VSA VSS zcap
x1[256] VSA VSS zcap
x1[255] VSA VSS zcap
x1[254] VSA VSS zcap
x1[253] VSA VSS zcap
x1[252] VSA VSS zcap
x1[251] VSA VSS zcap
x1[250] VSA VSS zcap
x1[249] VSA VSS zcap
x1[248] VSA VSS zcap
x1[247] VSA VSS zcap
x1[246] VSA VSS zcap
x1[245] VSA VSS zcap
x1[244] VSA VSS zcap
x1[243] VSA VSS zcap
x1[242] VSA VSS zcap
x1[241] VSA VSS zcap
x1[240] VSA VSS zcap
x1[239] VSA VSS zcap
x1[238] VSA VSS zcap
x1[237] VSA VSS zcap
x1[236] VSA VSS zcap
x1[235] VSA VSS zcap
x1[234] VSA VSS zcap
x1[233] VSA VSS zcap
x1[232] VSA VSS zcap
x1[231] VSA VSS zcap
x1[230] VSA VSS zcap
x1[229] VSA VSS zcap
x1[228] VSA VSS zcap
x1[227] VSA VSS zcap
x1[226] VSA VSS zcap
x1[225] VSA VSS zcap
x1[224] VSA VSS zcap
x1[223] VSA VSS zcap
x1[222] VSA VSS zcap
x1[221] VSA VSS zcap
x1[220] VSA VSS zcap
x1[219] VSA VSS zcap
x1[218] VSA VSS zcap
x1[217] VSA VSS zcap
x1[216] VSA VSS zcap
x1[215] VSA VSS zcap
x1[214] VSA VSS zcap
x1[213] VSA VSS zcap
x1[212] VSA VSS zcap
x1[211] VSA VSS zcap
x1[210] VSA VSS zcap
x1[209] VSA VSS zcap
x1[208] VSA VSS zcap
x1[207] VSA VSS zcap
x1[206] VSA VSS zcap
x1[205] VSA VSS zcap
x1[204] VSA VSS zcap
x1[203] VSA VSS zcap
x1[202] VSA VSS zcap
x1[201] VSA VSS zcap
x1[200] VSA VSS zcap
x1[199] VSA VSS zcap
x1[198] VSA VSS zcap
x1[197] VSA VSS zcap
x1[196] VSA VSS zcap
x1[195] VSA VSS zcap
x1[194] VSA VSS zcap
x1[193] VSA VSS zcap
x1[192] VSA VSS zcap
x1[191] VSA VSS zcap
x1[190] VSA VSS zcap
x1[189] VSA VSS zcap
x1[188] VSA VSS zcap
x1[187] VSA VSS zcap
x1[186] VSA VSS zcap
x1[185] VSA VSS zcap
x1[184] VSA VSS zcap
x1[183] VSA VSS zcap
x1[182] VSA VSS zcap
x1[181] VSA VSS zcap
x1[180] VSA VSS zcap
x1[179] VSA VSS zcap
x1[178] VSA VSS zcap
x1[177] VSA VSS zcap
x1[176] VSA VSS zcap
x1[175] VSA VSS zcap
x1[174] VSA VSS zcap
x1[173] VSA VSS zcap
x1[172] VSA VSS zcap
x1[171] VSA VSS zcap
x1[170] VSA VSS zcap
x1[169] VSA VSS zcap
x1[168] VSA VSS zcap
x1[167] VSA VSS zcap
x1[166] VSA VSS zcap
x1[165] VSA VSS zcap
x1[164] VSA VSS zcap
x1[163] VSA VSS zcap
x1[162] VSA VSS zcap
x1[161] VSA VSS zcap
x1[160] VSA VSS zcap
x1[159] VSA VSS zcap
x1[158] VSA VSS zcap
x1[157] VSA VSS zcap
x1[156] VSA VSS zcap
x1[155] VSA VSS zcap
x1[154] VSA VSS zcap
x1[153] VSA VSS zcap
x1[152] VSA VSS zcap
x1[151] VSA VSS zcap
x1[150] VSA VSS zcap
x1[149] VSA VSS zcap
x1[148] VSA VSS zcap
x1[147] VSA VSS zcap
x1[146] VSA VSS zcap
x1[145] VSA VSS zcap
x1[144] VSA VSS zcap
x1[143] VSA VSS zcap
x1[142] VSA VSS zcap
x1[141] VSA VSS zcap
x1[140] VSA VSS zcap
x1[139] VSA VSS zcap
x1[138] VSA VSS zcap
x1[137] VSA VSS zcap
x1[136] VSA VSS zcap
x1[135] VSA VSS zcap
x1[134] VSA VSS zcap
x1[133] VSA VSS zcap
x1[132] VSA VSS zcap
x1[131] VSA VSS zcap
x1[130] VSA VSS zcap
x1[129] VSA VSS zcap
x1[128] VSA VSS zcap
x1[127] VSA VSS zcap
x1[126] VSA VSS zcap
x1[125] VSA VSS zcap
x1[124] VSA VSS zcap
x1[123] VSA VSS zcap
x1[122] VSA VSS zcap
x1[121] VSA VSS zcap
x1[120] VSA VSS zcap
x1[119] VSA VSS zcap
x1[118] VSA VSS zcap
x1[117] VSA VSS zcap
x1[116] VSA VSS zcap
x1[115] VSA VSS zcap
x1[114] VSA VSS zcap
x1[113] VSA VSS zcap
x1[112] VSA VSS zcap
x1[111] VSA VSS zcap
x1[110] VSA VSS zcap
x1[109] VSA VSS zcap
x1[108] VSA VSS zcap
x1[107] VSA VSS zcap
x1[106] VSA VSS zcap
x1[105] VSA VSS zcap
x1[104] VSA VSS zcap
x1[103] VSA VSS zcap
x1[102] VSA VSS zcap
x1[101] VSA VSS zcap
x1[100] VSA VSS zcap
x1[99] VSA VSS zcap
x1[98] VSA VSS zcap
x1[97] VSA VSS zcap
x1[96] VSA VSS zcap
x1[95] VSA VSS zcap
x1[94] VSA VSS zcap
x1[93] VSA VSS zcap
x1[92] VSA VSS zcap
x1[91] VSA VSS zcap
x1[90] VSA VSS zcap
x1[89] VSA VSS zcap
x1[88] VSA VSS zcap
x1[87] VSA VSS zcap
x1[86] VSA VSS zcap
x1[85] VSA VSS zcap
x1[84] VSA VSS zcap
x1[83] VSA VSS zcap
x1[82] VSA VSS zcap
x1[81] VSA VSS zcap
x1[80] VSA VSS zcap
x1[79] VSA VSS zcap
x1[78] VSA VSS zcap
x1[77] VSA VSS zcap
x1[76] VSA VSS zcap
x1[75] VSA VSS zcap
x1[74] VSA VSS zcap
x1[73] VSA VSS zcap
x1[72] VSA VSS zcap
x1[71] VSA VSS zcap
x1[70] VSA VSS zcap
x1[69] VSA VSS zcap
x1[68] VSA VSS zcap
x1[67] VSA VSS zcap
x1[66] VSA VSS zcap
x1[65] VSA VSS zcap
x1[64] VSA VSS zcap
x1[63] VSA VSS zcap
x1[62] VSA VSS zcap
x1[61] VSA VSS zcap
x1[60] VSA VSS zcap
x1[59] VSA VSS zcap
x1[58] VSA VSS zcap
x1[57] VSA VSS zcap
x1[56] VSA VSS zcap
x1[55] VSA VSS zcap
x1[54] VSA VSS zcap
x1[53] VSA VSS zcap
x1[52] VSA VSS zcap
x1[51] VSA VSS zcap
x1[50] VSA VSS zcap
x1[49] VSA VSS zcap
x1[48] VSA VSS zcap
x1[47] VSA VSS zcap
x1[46] VSA VSS zcap
x1[45] VSA VSS zcap
x1[44] VSA VSS zcap
x1[43] VSA VSS zcap
x1[42] VSA VSS zcap
x1[41] VSA VSS zcap
x1[40] VSA VSS zcap
x1[39] VSA VSS zcap
x1[38] VSA VSS zcap
x1[37] VSA VSS zcap
x1[36] VSA VSS zcap
x1[35] VSA VSS zcap
x1[34] VSA VSS zcap
x1[33] VSA VSS zcap
x1[32] VSA VSS zcap
x1[31] VSA VSS zcap
x1[30] VSA VSS zcap
x1[29] VSA VSS zcap
x1[28] VSA VSS zcap
x1[27] VSA VSS zcap
x1[26] VSA VSS zcap
x1[25] VSA VSS zcap
x1[24] VSA VSS zcap
x1[23] VSA VSS zcap
x1[22] VSA VSS zcap
x1[21] VSA VSS zcap
x1[20] VSA VSS zcap
x1[19] VSA VSS zcap
x1[18] VSA VSS zcap
x1[17] VSA VSS zcap
x1[16] VSA VSS zcap
x1[15] VSA VSS zcap
x1[14] VSA VSS zcap
x1[13] VSA VSS zcap
x1[12] VSA VSS zcap
x1[11] VSA VSS zcap
x1[10] VSA VSS zcap
x1[9] VSA VSS zcap
x1[8] VSA VSS zcap
x1[7] VSA VSS zcap
x1[6] VSA VSS zcap
x1[5] VSA VSS zcap
x1[4] VSA VSS zcap
x1[3] VSA VSS zcap
x1[2] VSA VSS zcap
x1[1] VSA VSS zcap
x1[0] VSA VSS zcap
**.ends
.end
